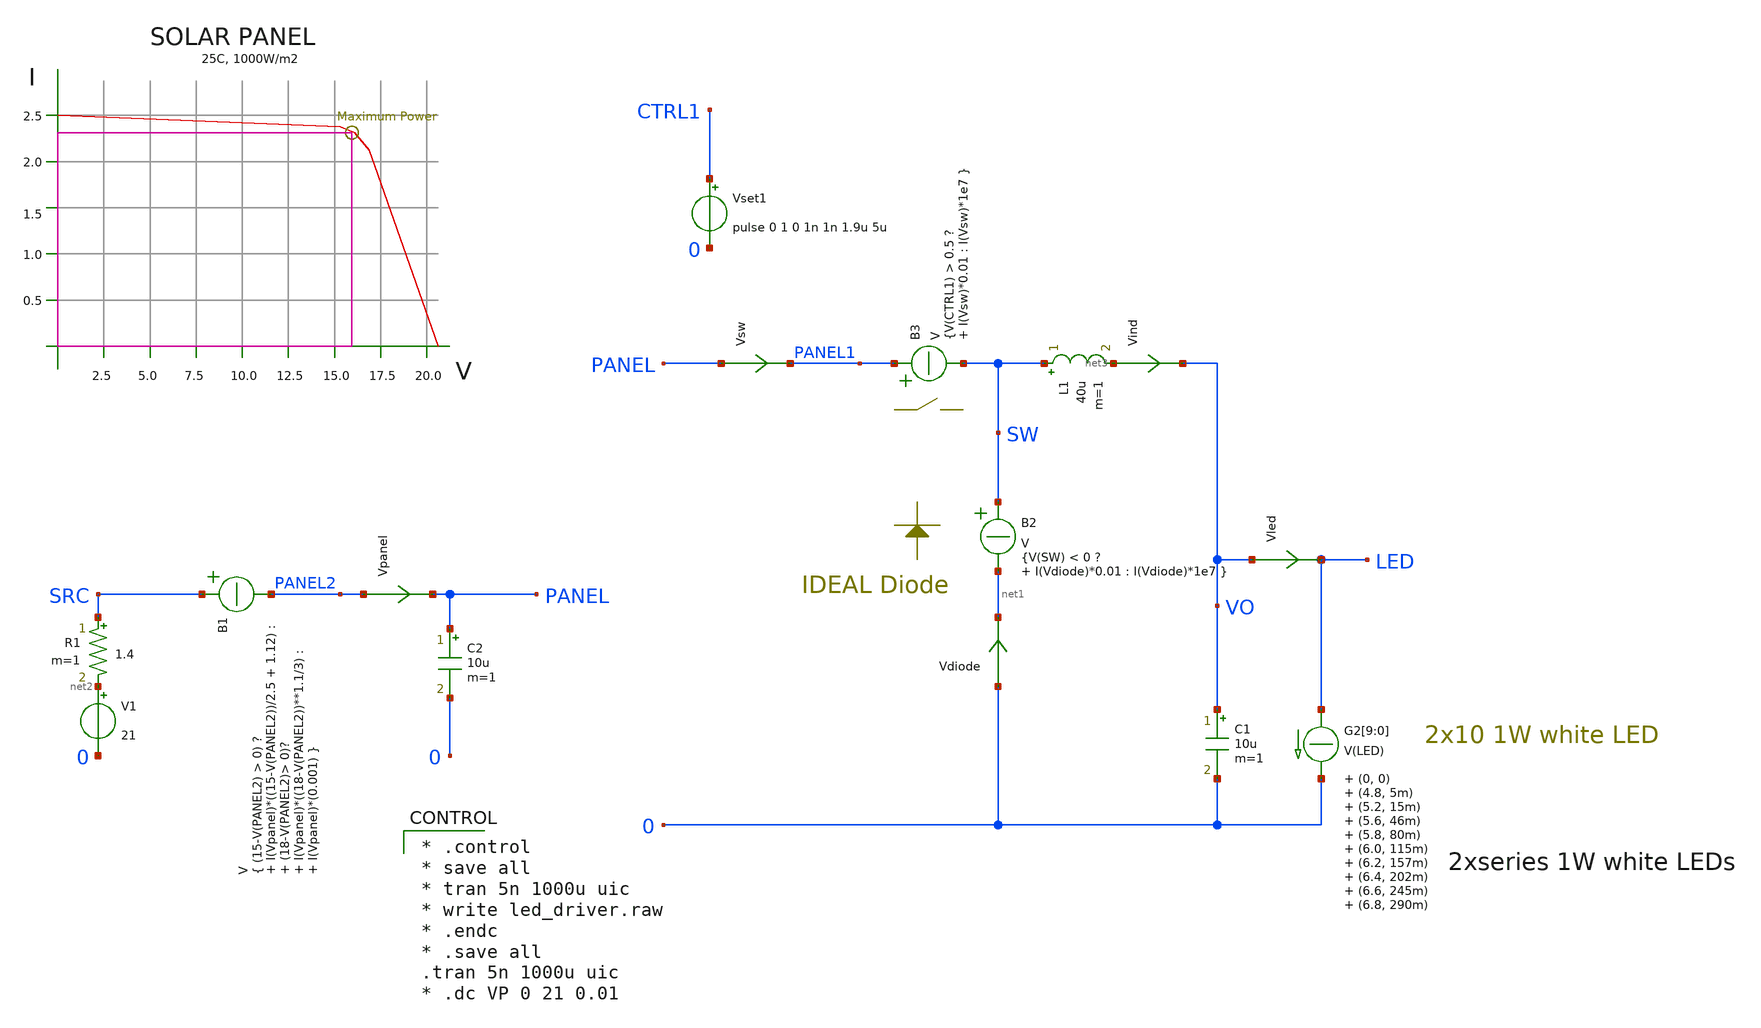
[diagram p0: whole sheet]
** sch_path: xschem_library/ngspice/solar_panel_xyce.sch
**.subckt solar_panel_xyce
V1 net2 0 21
R1 SRC net2 1.4 m=1
Vled VO LED 0
.save i(vled)
L1 SW net3 40u m=1
C1 VO 0 10u m=1
Vpanel PANEL2 PANEL 0
.save i(vpanel)
Vset1 CTRL1 0 pulse 0 1 0 1n 1n 1.9u 5u
Vind net3 VO 0
.save i(vind)
C2 PANEL 0 10u m=1
G2[9] LED 0 TABLE { V(LED) } = (0, 0) (4.8, 5m) (5.2, 15m) (5.6, 46m) (5.8, 80m) (6.0, 115m) (6.2, 157m)
+ (6.4, 202m) (6.6, 245m) (6.8, 290m) (7.0, 337m) (7.2, 395m) (7.4, 470m) (8.0, 750m)
G2[8] LED 0 TABLE { V(LED) } = (0, 0) (4.8, 5m) (5.2, 15m) (5.6, 46m) (5.8, 80m) (6.0, 115m) (6.2, 157m)
+ (6.4, 202m) (6.6, 245m) (6.8, 290m) (7.0, 337m) (7.2, 395m) (7.4, 470m) (8.0, 750m)
G2[7] LED 0 TABLE { V(LED) } = (0, 0) (4.8, 5m) (5.2, 15m) (5.6, 46m) (5.8, 80m) (6.0, 115m) (6.2, 157m)
+ (6.4, 202m) (6.6, 245m) (6.8, 290m) (7.0, 337m) (7.2, 395m) (7.4, 470m) (8.0, 750m)
G2[6] LED 0 TABLE { V(LED) } = (0, 0) (4.8, 5m) (5.2, 15m) (5.6, 46m) (5.8, 80m) (6.0, 115m) (6.2, 157m)
+ (6.4, 202m) (6.6, 245m) (6.8, 290m) (7.0, 337m) (7.2, 395m) (7.4, 470m) (8.0, 750m)
G2[5] LED 0 TABLE { V(LED) } = (0, 0) (4.8, 5m) (5.2, 15m) (5.6, 46m) (5.8, 80m) (6.0, 115m) (6.2, 157m)
+ (6.4, 202m) (6.6, 245m) (6.8, 290m) (7.0, 337m) (7.2, 395m) (7.4, 470m) (8.0, 750m)
G2[4] LED 0 TABLE { V(LED) } = (0, 0) (4.8, 5m) (5.2, 15m) (5.6, 46m) (5.8, 80m) (6.0, 115m) (6.2, 157m)
+ (6.4, 202m) (6.6, 245m) (6.8, 290m) (7.0, 337m) (7.2, 395m) (7.4, 470m) (8.0, 750m)
G2[3] LED 0 TABLE { V(LED) } = (0, 0) (4.8, 5m) (5.2, 15m) (5.6, 46m) (5.8, 80m) (6.0, 115m) (6.2, 157m)
+ (6.4, 202m) (6.6, 245m) (6.8, 290m) (7.0, 337m) (7.2, 395m) (7.4, 470m) (8.0, 750m)
G2[2] LED 0 TABLE { V(LED) } = (0, 0) (4.8, 5m) (5.2, 15m) (5.6, 46m) (5.8, 80m) (6.0, 115m) (6.2, 157m)
+ (6.4, 202m) (6.6, 245m) (6.8, 290m) (7.0, 337m) (7.2, 395m) (7.4, 470m) (8.0, 750m)
G2[1] LED 0 TABLE { V(LED) } = (0, 0) (4.8, 5m) (5.2, 15m) (5.6, 46m) (5.8, 80m) (6.0, 115m) (6.2, 157m)
+ (6.4, 202m) (6.6, 245m) (6.8, 290m) (7.0, 337m) (7.2, 395m) (7.4, 470m) (8.0, 750m)
G2[0] LED 0 TABLE { V(LED) } = (0, 0) (4.8, 5m) (5.2, 15m) (5.6, 46m) (5.8, 80m) (6.0, 115m) (6.2, 157m)
+ (6.4, 202m) (6.6, 245m) (6.8, 290m) (7.0, 337m) (7.2, 395m) (7.4, 470m) (8.0, 750m)
Vsw PANEL PANEL1 0
.save i(vsw)
Vdiode 0 net1 0
.save i(vdiode)
B1 SRC PANEL2 V = { (15-V(PANEL2) > 0) ? I(Vpanel)*((15-V(PANEL2))/2.5 + 1.12) : (18-V(PANEL2)> 0)? I(Vpanel)*((18-V(PANEL2))**1.1/3) : I(Vpanel)*(0.001) }
B2 SW net1 V = {V(SW) < 0 ? I(Vdiode)*0.01 : I(Vdiode)*1e7 }
B3 PANEL1 SW V = {V(CTRL1) > 0.5 ? I(Vsw)*0.01 : I(Vsw)*1e7 }
**** begin user architecture code

* .control
* save all
* tran 5n 1000u uic
* write led_driver.raw
* .endc
* .save all
.tran 5n 1000u uic
* .dc VP 0 21 0.01



.MODEL DIODE D(IS=1.139e-08 RS=0.99 CJO=9.3e-12 VJ=1.6 M=0.411 BV=30 EG=0.7 )
.MODEL swmod SW(VT=0.1 VH=0.01 RON=0.01 ROFF=10000000)


**** end user architecture code
**.ends
.end
